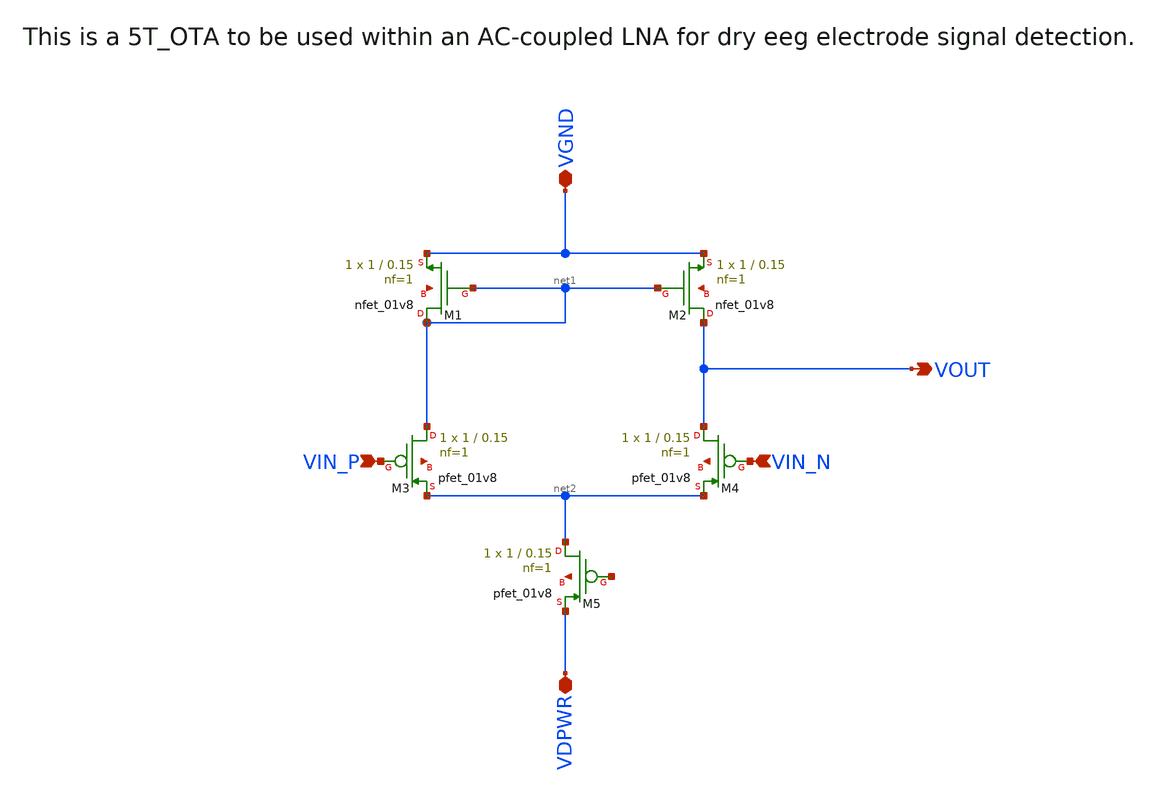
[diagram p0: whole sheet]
** sch_path: xschem/5t_ota.sch
**.subckt 5t_ota VGND VIN_N VIN_P VDPWR VOUT
*.iopin VGND
*.ipin VIN_N
*.ipin VIN_P
*.iopin VDPWR
*.opin VOUT
XM1 net1 net1 VGND net3 sky130_fd_pr__nfet_01v8 L=0.15 W=1 nf=1 ad='int((1 + 1)/2) * 1 / 1 * 0.29' as='int((1 + 2)/2) * 1 / 1 * 0.29'
+ pd='2*int((1 + 1)/2) * (1 / 1 + 0.29)' ps='2*int((1 + 2)/2) * (1 / 1 + 0.29)' nrd='0.29 / 1 ' nrs='0.29 / 1 '
+ sa=0 sb=0 sd=0 mult=1 m=1
XM2 VOUT net1 VGND net4 sky130_fd_pr__nfet_01v8 L=0.15 W=1 nf=1 ad='int((1 + 1)/2) * 1 / 1 * 0.29' as='int((1 + 2)/2) * 1 / 1 * 0.29'
+ pd='2*int((1 + 1)/2) * (1 / 1 + 0.29)' ps='2*int((1 + 2)/2) * (1 / 1 + 0.29)' nrd='0.29 / 1 ' nrs='0.29 / 1 '
+ sa=0 sb=0 sd=0 mult=1 m=1
XM3 net1 VIN_P net2 net5 sky130_fd_pr__pfet_01v8 L=0.15 W=1 nf=1 ad='int((1 + 1)/2) * 1 / 1 * 0.29' as='int((1 + 2)/2) * 1 / 1 * 0.29'
+ pd='2*int((1 + 1)/2) * (1 / 1 + 0.29)' ps='2*int((1 + 2)/2) * (1 / 1 + 0.29)' nrd='0.29 / 1 ' nrs='0.29 / 1 '
+ sa=0 sb=0 sd=0 mult=1 m=1
XM4 VOUT VIN_N net2 net6 sky130_fd_pr__pfet_01v8 L=0.15 W=1 nf=1 ad='int((1 + 1)/2) * 1 / 1 * 0.29' as='int((1 + 2)/2) * 1 / 1 * 0.29'
+ pd='2*int((1 + 1)/2) * (1 / 1 + 0.29)' ps='2*int((1 + 2)/2) * (1 / 1 + 0.29)' nrd='0.29 / 1 ' nrs='0.29 / 1 '
+ sa=0 sb=0 sd=0 mult=1 m=1
XM5 net2 net7 VDPWR net8 sky130_fd_pr__pfet_01v8 L=0.15 W=1 nf=1 ad='int((1 + 1)/2) * 1 / 1 * 0.29' as='int((1 + 2)/2) * 1 / 1 * 0.29'
+ pd='2*int((1 + 1)/2) * (1 / 1 + 0.29)' ps='2*int((1 + 2)/2) * (1 / 1 + 0.29)' nrd='0.29 / 1 ' nrs='0.29 / 1 '
+ sa=0 sb=0 sd=0 mult=1 m=1
**.ends
.end
